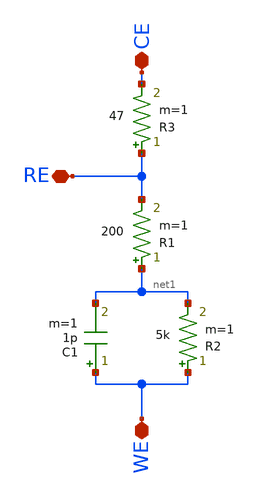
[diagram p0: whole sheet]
** sch_path: Schematics/POTENCIOSTAT/ECH_sensor.sch
**.subckt ECH_sensor CE RE WE
*.iopin CE
*.iopin RE
*.iopin WE
R3 RE CE 47 m=1
R1 net1 RE 200 m=1
C1 WE net1 1p m=1
R2 WE net1 5k m=1
**.ends
.end
